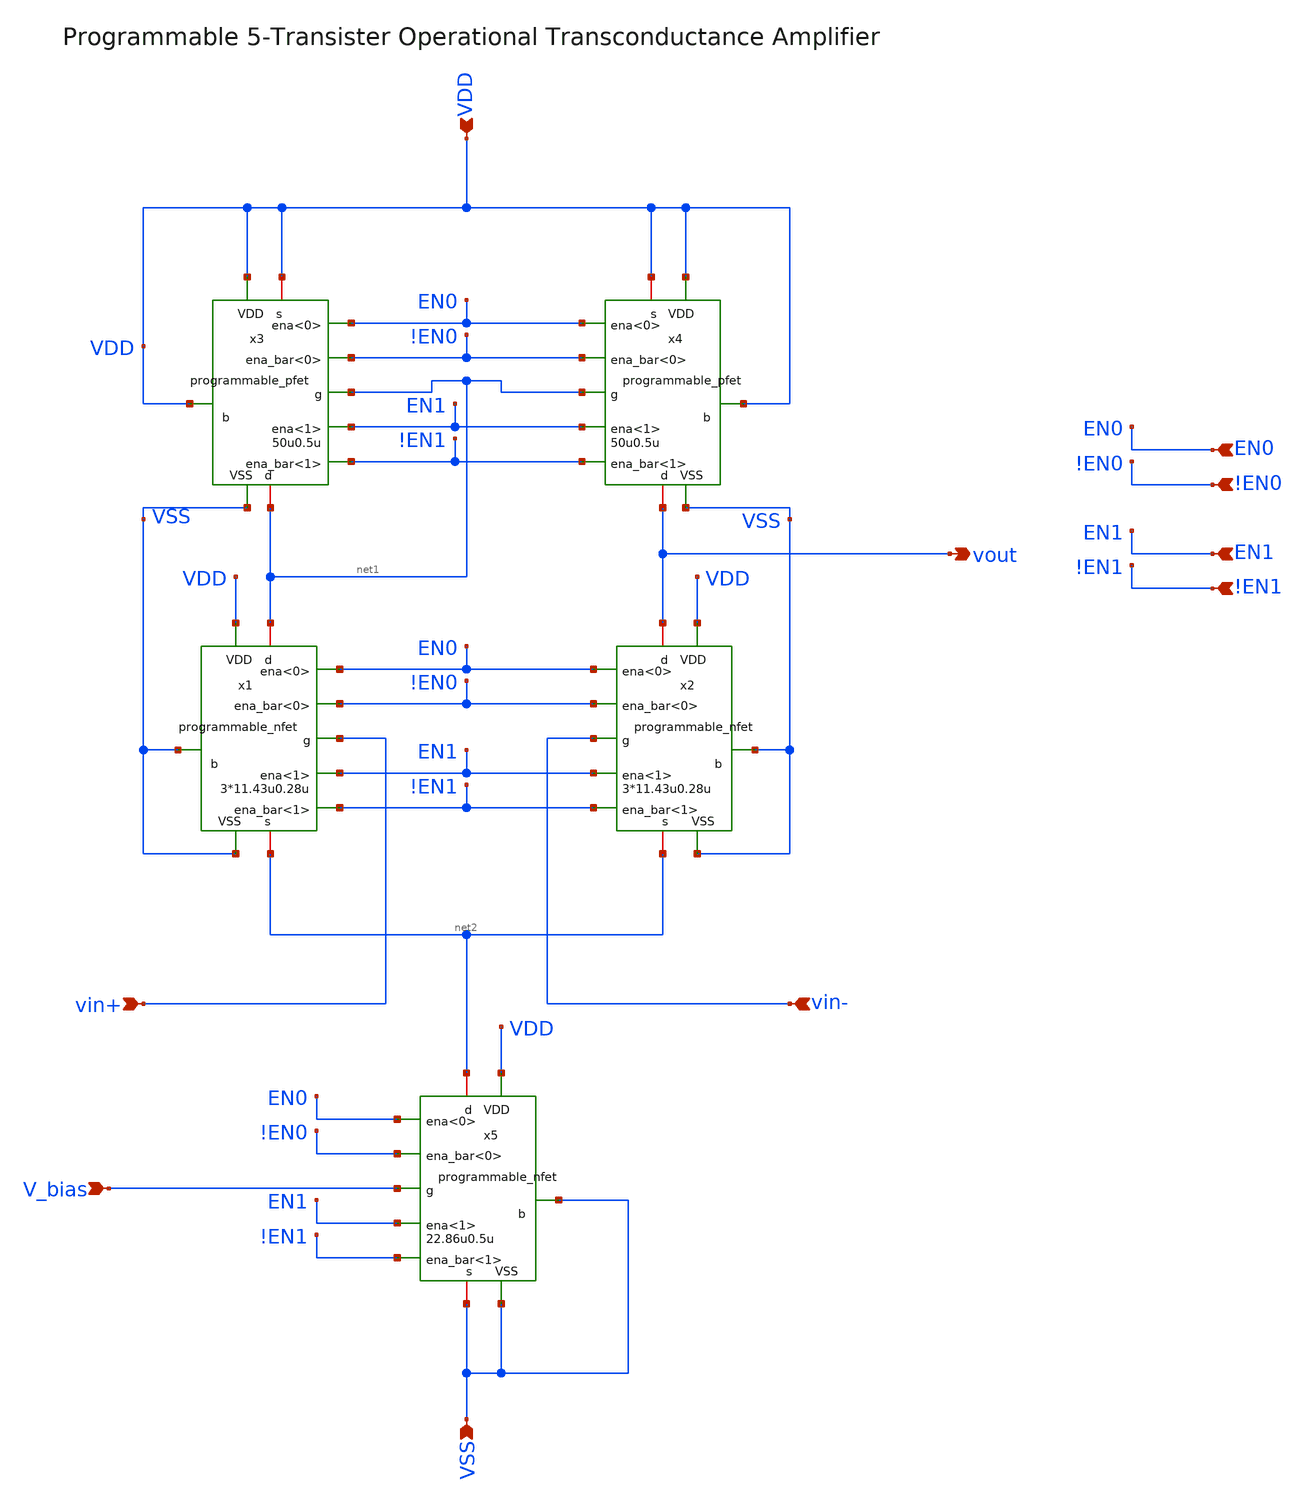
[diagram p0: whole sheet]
** sch_path: designs/libs/core_amps/ota_5t/programmable_5tOTA_3.sch
**.subckt programmable_5tOTA_3 VDD vout vin+ vin- V_bias VSS EN0 !EN0 EN1 !EN1
*.ipin VDD
*.opin vout
*.ipin vin+
*.ipin vin-
*.ipin V_bias
*.ipin VSS
*.ipin EN0
*.ipin !EN0
*.ipin EN1
*.ipin !EN1
x3 net1 VDD net1 VDD !EN0 VDD !EN1 EN0 EN1 VSS programmable_pfet width=50u length=0.5u
x1 net1 VSS vin+ net2 !EN0 VDD !EN1 EN0 EN1 VSS programmable_nfet width=3*11.43u length=0.28u
x5 net2 VSS V_bias VSS !EN0 VDD !EN1 EN0 EN1 VSS programmable_nfet width=22.86u length=0.5u
x4 vout VDD net1 VDD !EN0 VDD !EN1 EN0 EN1 VSS programmable_pfet width=50u length=0.5u
x2 vout VSS vin- net2 !EN0 VDD !EN1 EN0 EN1 VSS programmable_nfet width=3*11.43u length=0.28u
**.ends
.end
